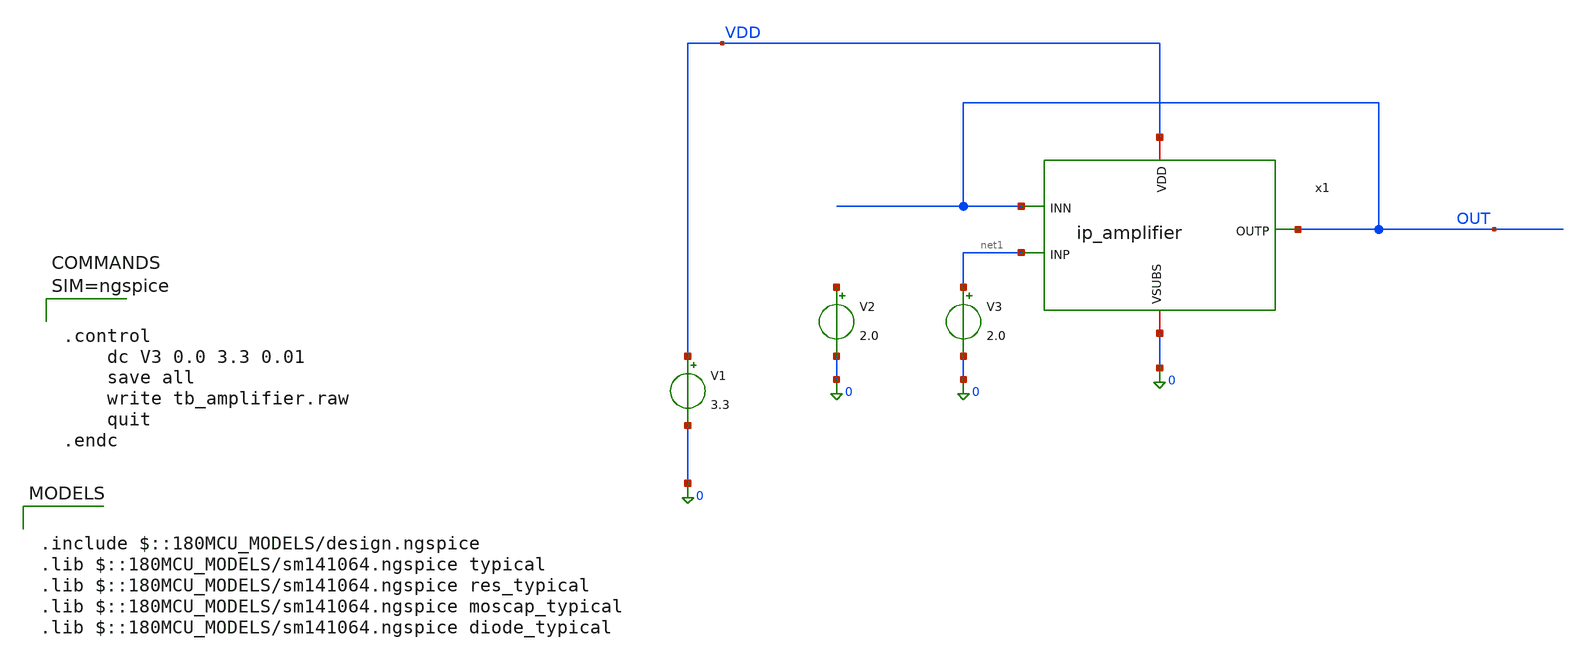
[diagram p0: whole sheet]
** sch_path: xschem/tb_amplifier.sch
**.subckt tb_amplifier
V1 VDD 0 3.3
x1 VDD OUT net1 OUT 0 ip_amplifier
V3 net1 0 2.0
V2 net2 0 2.0
**** begin user architecture code

.include $::180MCU_MODELS/design.ngspice
.lib $::180MCU_MODELS/sm141064.ngspice typical
.lib $::180MCU_MODELS/sm141064.ngspice res_typical
.lib $::180MCU_MODELS/sm141064.ngspice moscap_typical
.lib $::180MCU_MODELS/sm141064.ngspice diode_typical




.control
	dc V3 0.0 3.3 0.01
	save all
	write tb_amplifier.raw
	quit
.endc



**** end user architecture code
**.ends

* expanding   symbol:  ip_amplifier.sym # of pins=5
** sym_path: xschem/ip_amplifier.sym
** sch_path: xschem/ip_amplifier.sch
.subckt ip_amplifier VDD OUTP INP INN VSUBS
*.iopin VDD
*.iopin VSUBS
*.opin OUTP
*.ipin INP
*.ipin INN
XM1 net6 net7 VDD VDD pfet_03v3 L=0.5u W=3.0u nf=1 ad='int((nf+1)/2) * W/nf * 0.18u' as='int((nf+2)/2) * W/nf * 0.18u'
+ pd='2*int((nf+1)/2) * (W/nf + 0.18u)' ps='2*int((nf+2)/2) * (W/nf + 0.18u)' nrd='0.18u / W' nrs='0.18u / W'
+ sa=0 sb=0 sd=0 m=1 par=1
XM2 net4 net2 net3 VSUBS nfet_03v3 L=2.0u W=10u nf=1 ad='int((nf+1)/2) * W/nf * 0.18u' as='int((nf+2)/2) * W/nf * 0.18u'
+ pd='2*int((nf+1)/2) * (W/nf + 0.18u)' ps='2*int((nf+2)/2) * (W/nf + 0.18u)' nrd='0.18u / W' nrs='0.18u / W'
+ sa=0 sb=0 sd=0 m=1 par=1
XM3 net3 net2 VSUBS VSUBS nfet_03v3 L=0.5u W=1.0u nf=1 ad='int((nf+1)/2) * W/nf * 0.18u' as='int((nf+2)/2) * W/nf * 0.18u'
+ pd='2*int((nf+1)/2) * (W/nf + 0.18u)' ps='2*int((nf+2)/2) * (W/nf + 0.18u)' nrd='0.18u / W' nrs='0.18u / W'
+ sa=0 sb=0 sd=0 m=1 par=1
XM4 net1 net2 VSUBS VSUBS nfet_03v3 L=0.5u W=1.0u nf=1 ad='int((nf+1)/2) * W/nf * 0.18u' as='int((nf+2)/2) * W/nf * 0.18u'
+ pd='2*int((nf+1)/2) * (W/nf + 0.18u)' ps='2*int((nf+2)/2) * (W/nf + 0.18u)' nrd='0.18u / W' nrs='0.18u / W'
+ sa=0 sb=0 sd=0 m=1 par=1
XM5 net5 net7 VDD VDD pfet_03v3 L=0.5u W=3.0u nf=1 ad='int((nf+1)/2) * W/nf * 0.18u' as='int((nf+2)/2) * W/nf * 0.18u'
+ pd='2*int((nf+1)/2) * (W/nf + 0.18u)' ps='2*int((nf+2)/2) * (W/nf + 0.18u)' nrd='0.18u / W' nrs='0.18u / W'
+ sa=0 sb=0 sd=0 m=1 par=1
XM6 net9 net7 net5 VDD pfet_03v3 L=2.0u W=10.0u nf=1 ad='int((nf+1)/2) * W/nf * 0.18u' as='int((nf+2)/2) * W/nf * 0.18u'
+ pd='2*int((nf+1)/2) * (W/nf + 0.18u)' ps='2*int((nf+2)/2) * (W/nf + 0.18u)' nrd='0.18u / W' nrs='0.18u / W'
+ sa=0 sb=0 sd=0 m=1 par=1
XM17 net7 net7 net6 VDD pfet_03v3 L=2.0u W=10.0u nf=1 ad='int((nf+1)/2) * W/nf * 0.18u' as='int((nf+2)/2) * W/nf * 0.18u'
+ pd='2*int((nf+1)/2) * (W/nf + 0.18u)' ps='2*int((nf+2)/2) * (W/nf + 0.18u)' nrd='0.18u / W' nrs='0.18u / W'
+ sa=0 sb=0 sd=0 m=1 par=1
XM18 net2 net2 net1 VSUBS nfet_03v3 L=2.0u W=10u nf=1 ad='int((nf+1)/2) * W/nf * 0.18u' as='int((nf+2)/2) * W/nf * 0.18u'
+ pd='2*int((nf+1)/2) * (W/nf + 0.18u)' ps='2*int((nf+2)/2) * (W/nf + 0.18u)' nrd='0.18u / W' nrs='0.18u / W'
+ sa=0 sb=0 sd=0 m=1 par=1
R1 VDD net8 100k m=1
Vmeas1 net8 net2 0
Vmeas8 net7 net4 0
XM19 net10 INP net9 VDD pfet_03v3 L=2.0u W=10.0u nf=1 ad='int((nf+1)/2) * W/nf * 0.18u' as='int((nf+2)/2) * W/nf * 0.18u'
+ pd='2*int((nf+1)/2) * (W/nf + 0.18u)' ps='2*int((nf+2)/2) * (W/nf + 0.18u)' nrd='0.18u / W' nrs='0.18u / W'
+ sa=0 sb=0 sd=0 m=1 par=1
XM20 net11 INN net9 VDD pfet_03v3 L=2.0u W=10.0u nf=1 ad='int((nf+1)/2) * W/nf * 0.18u' as='int((nf+2)/2) * W/nf * 0.18u'
+ pd='2*int((nf+1)/2) * (W/nf + 0.18u)' ps='2*int((nf+2)/2) * (W/nf + 0.18u)' nrd='0.18u / W' nrs='0.18u / W'
+ sa=0 sb=0 sd=0 m=1 par=1
R2 net16 net13 50k m=1
XM11 net12 net2 net10 VSUBS nfet_03v3 L=2.0u W=10u nf=1 ad='int((nf+1)/2) * W/nf * 0.18u' as='int((nf+2)/2) * W/nf * 0.18u'
+ pd='2*int((nf+1)/2) * (W/nf + 0.18u)' ps='2*int((nf+2)/2) * (W/nf + 0.18u)' nrd='0.18u / W' nrs='0.18u / W'
+ sa=0 sb=0 sd=0 m=1 par=1
XM12 net10 net2 VSUBS VSUBS nfet_03v3 L=0.5u W=1.0u nf=1 ad='int((nf+1)/2) * W/nf * 0.18u' as='int((nf+2)/2) * W/nf * 0.18u'
+ pd='2*int((nf+1)/2) * (W/nf + 0.18u)' ps='2*int((nf+2)/2) * (W/nf + 0.18u)' nrd='0.18u / W' nrs='0.18u / W'
+ sa=0 sb=0 sd=0 m=1 par=1
XM21 net11 net2 VSUBS VSUBS nfet_03v3 L=0.5u W=1.0u nf=1 ad='int((nf+1)/2) * W/nf * 0.18u' as='int((nf+2)/2) * W/nf * 0.18u'
+ pd='2*int((nf+1)/2) * (W/nf + 0.18u)' ps='2*int((nf+2)/2) * (W/nf + 0.18u)' nrd='0.18u / W' nrs='0.18u / W'
+ sa=0 sb=0 sd=0 m=1 par=1
XM22 net13 net2 net11 VSUBS nfet_03v3 L=2.0u W=10u nf=1 ad='int((nf+1)/2) * W/nf * 0.18u' as='int((nf+2)/2) * W/nf * 0.18u'
+ pd='2*int((nf+1)/2) * (W/nf + 0.18u)' ps='2*int((nf+2)/2) * (W/nf + 0.18u)' nrd='0.18u / W' nrs='0.18u / W'
+ sa=0 sb=0 sd=0 m=1 par=1
XM7 net15 net16 VDD VDD pfet_03v3 L=0.5u W=3.0u nf=1 ad='int((nf+1)/2) * W/nf * 0.18u' as='int((nf+2)/2) * W/nf * 0.18u'
+ pd='2*int((nf+1)/2) * (W/nf + 0.18u)' ps='2*int((nf+2)/2) * (W/nf + 0.18u)' nrd='0.18u / W' nrs='0.18u / W'
+ sa=0 sb=0 sd=0 m=1 par=1
XM8 net14 net16 VDD VDD pfet_03v3 L=0.5u W=3.0u nf=1 ad='int((nf+1)/2) * W/nf * 0.18u' as='int((nf+2)/2) * W/nf * 0.18u'
+ pd='2*int((nf+1)/2) * (W/nf + 0.18u)' ps='2*int((nf+2)/2) * (W/nf + 0.18u)' nrd='0.18u / W' nrs='0.18u / W'
+ sa=0 sb=0 sd=0 m=1 par=1
XM9 net17 net13 net14 VDD pfet_03v3 L=2.0u W=10.0u nf=1 ad='int((nf+1)/2) * W/nf * 0.18u' as='int((nf+2)/2) * W/nf * 0.18u'
+ pd='2*int((nf+1)/2) * (W/nf + 0.18u)' ps='2*int((nf+2)/2) * (W/nf + 0.18u)' nrd='0.18u / W' nrs='0.18u / W'
+ sa=0 sb=0 sd=0 m=1 par=1
XM10 net16 net13 net15 VDD pfet_03v3 L=2.0u W=10.0u nf=1 ad='int((nf+1)/2) * W/nf * 0.18u' as='int((nf+2)/2) * W/nf * 0.18u'
+ pd='2*int((nf+1)/2) * (W/nf + 0.18u)' ps='2*int((nf+2)/2) * (W/nf + 0.18u)' nrd='0.18u / W' nrs='0.18u / W'
+ sa=0 sb=0 sd=0 m=1 par=1
XM13 net20 net2 VSUBS VSUBS nfet_03v3 L=0.5u W=1.0u nf=1 ad='int((nf+1)/2) * W/nf * 0.18u' as='int((nf+2)/2) * W/nf * 0.18u'
+ pd='2*int((nf+1)/2) * (W/nf + 0.18u)' ps='2*int((nf+2)/2) * (W/nf + 0.18u)' nrd='0.18u / W' nrs='0.18u / W'
+ sa=0 sb=0 sd=0 m=1 par=1
XM14 net12 net20 net17 VDD pfet_03v3 L=2.0u W=10.0u nf=1 ad='int((nf+1)/2) * W/nf * 0.18u' as='int((nf+2)/2) * W/nf * 0.18u'
+ pd='2*int((nf+1)/2) * (W/nf + 0.18u)' ps='2*int((nf+2)/2) * (W/nf + 0.18u)' nrd='0.18u / W' nrs='0.18u / W'
+ sa=0 sb=0 sd=0 m=1 par=1
XM15 net19 net19 VDD VDD pfet_03v3 L=0.5u W=3.0u nf=1 ad='int((nf+1)/2) * W/nf * 0.18u' as='int((nf+2)/2) * W/nf * 0.18u'
+ pd='2*int((nf+1)/2) * (W/nf + 0.18u)' ps='2*int((nf+2)/2) * (W/nf + 0.18u)' nrd='0.18u / W' nrs='0.18u / W'
+ sa=0 sb=0 sd=0 m=1 par=1
XM16 net18 net7 VDD VDD pfet_03v3 L=0.5u W=3.0u nf=1 ad='int((nf+1)/2) * W/nf * 0.18u' as='int((nf+2)/2) * W/nf * 0.18u'
+ pd='2*int((nf+1)/2) * (W/nf + 0.18u)' ps='2*int((nf+2)/2) * (W/nf + 0.18u)' nrd='0.18u / W' nrs='0.18u / W'
+ sa=0 sb=0 sd=0 m=1 par=1
XM24 net20 net20 net19 VDD pfet_03v3 L=2.0u W=10.0u nf=1 ad='int((nf+1)/2) * W/nf * 0.18u' as='int((nf+2)/2) * W/nf * 0.18u'
+ pd='2*int((nf+1)/2) * (W/nf + 0.18u)' ps='2*int((nf+2)/2) * (W/nf + 0.18u)' nrd='0.18u / W' nrs='0.18u / W'
+ sa=0 sb=0 sd=0 m=1 par=1
XM23 net12 net18 net17 VDD pfet_03v3 L=2.0u W=10.0u nf=1 ad='int((nf+1)/2) * W/nf * 0.18u' as='int((nf+2)/2) * W/nf * 0.18u'
+ pd='2*int((nf+1)/2) * (W/nf + 0.18u)' ps='2*int((nf+2)/2) * (W/nf + 0.18u)' nrd='0.18u / W' nrs='0.18u / W'
+ sa=0 sb=0 sd=0 m=1 par=1
XM25 net18 net18 net21 VSUBS nfet_03v3 L=0.5u W=1.0u nf=1 ad='int((nf+1)/2) * W/nf * 0.18u' as='int((nf+2)/2) * W/nf * 0.18u'
+ pd='2*int((nf+1)/2) * (W/nf + 0.18u)' ps='2*int((nf+2)/2) * (W/nf + 0.18u)' nrd='0.18u / W' nrs='0.18u / W'
+ sa=0 sb=0 sd=0 m=1 par=1
XM26 net21 net21 VSUBS VSUBS nfet_03v3 L=0.5u W=1.0u nf=1 ad='int((nf+1)/2) * W/nf * 0.18u' as='int((nf+2)/2) * W/nf * 0.18u'
+ pd='2*int((nf+1)/2) * (W/nf + 0.18u)' ps='2*int((nf+2)/2) * (W/nf + 0.18u)' nrd='0.18u / W' nrs='0.18u / W'
+ sa=0 sb=0 sd=0 m=1 par=1
C1 net17 OUTP 1p m=1
C2 OUTP net12 1p m=1
XM27 OUTP net17 VDD VDD pfet_03v3 L=0.5u W=3.0u nf=1 ad='int((nf+1)/2) * W/nf * 0.18u' as='int((nf+2)/2) * W/nf * 0.18u'
+ pd='2*int((nf+1)/2) * (W/nf + 0.18u)' ps='2*int((nf+2)/2) * (W/nf + 0.18u)' nrd='0.18u / W' nrs='0.18u / W'
+ sa=0 sb=0 sd=0 m=1 par=1
XM28 OUTP net12 VSUBS VSUBS nfet_03v3 L=0.5u W=1.0u nf=1 ad='int((nf+1)/2) * W/nf * 0.18u' as='int((nf+2)/2) * W/nf * 0.18u'
+ pd='2*int((nf+1)/2) * (W/nf + 0.18u)' ps='2*int((nf+2)/2) * (W/nf + 0.18u)' nrd='0.18u / W' nrs='0.18u / W'
+ sa=0 sb=0 sd=0 m=1 par=1
.ends

.end
